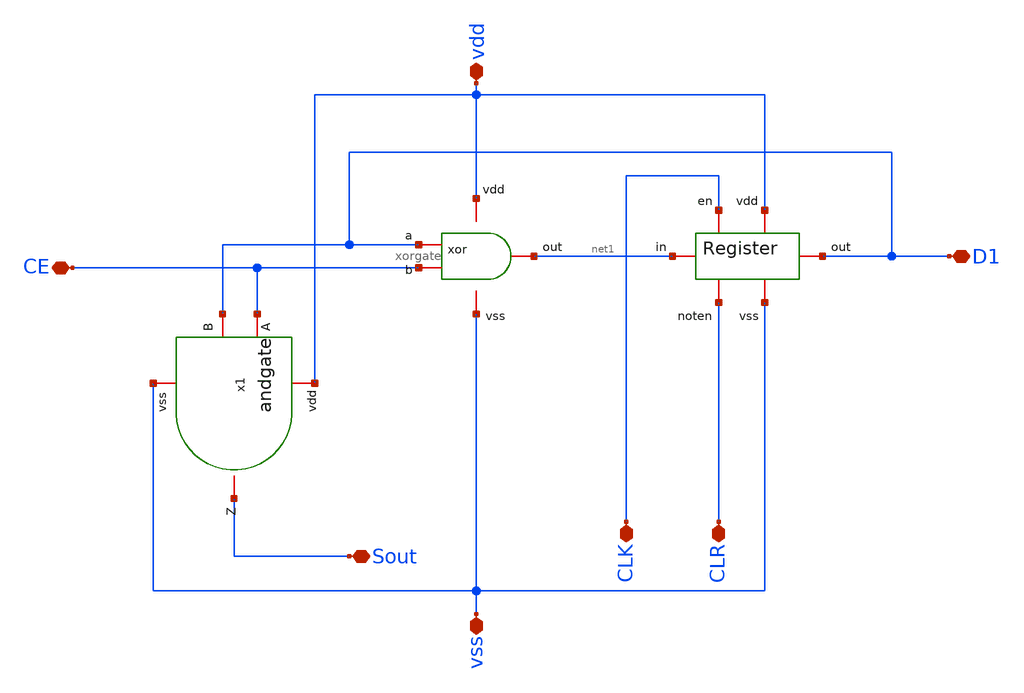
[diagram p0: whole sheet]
** sch_path: design/blocks/count1bit/schematic/count1bit.sch
**.subckt count1bit CE CLK CLR Sout vdd vss D1
*.iopin CE
*.iopin CLK
*.iopin CLR
*.iopin Sout
*.iopin vdd
*.iopin vss
*.iopin D1
x1 vdd CE D1 Sout vss andgate
x2 D1 vdd CE vss net1 xorgate
x3 CLK CLR vss vdd D1 net1 register
**.ends
.end
